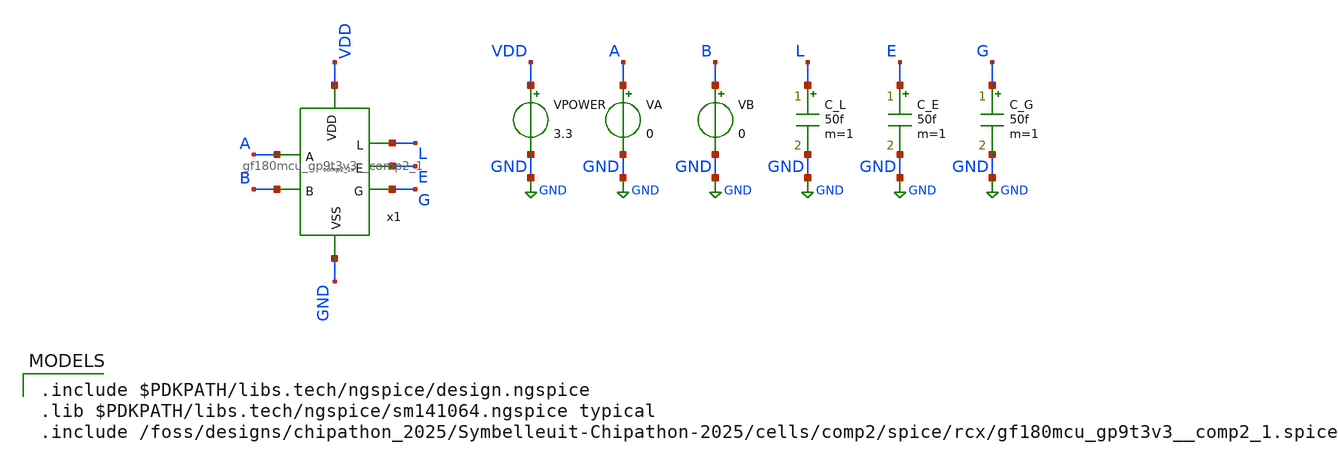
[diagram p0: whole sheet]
** sch_path: cells/comp2/cace/templates/comp2_tb_qpower.sch
**.subckt comp2_tb_qpower
x1 VDD L A E G B GND gf180mcu_gp9t3v3__comp2_1
VPOWER VDD GND 3.3
.save i(vpower)
VA A GND 0
VB B GND 0
C_L L GND 50f m=1
C_E E GND 50f m=1
C_G G GND 50f m=1
**** begin user architecture code

.include $PDKPATH/libs.tech/ngspice/design.ngspice
.lib $PDKPATH/libs.tech/ngspice/sm141064.ngspice typical
.include /foss/designs/chipathon_2025/Symbelleuit-Chipathon-2025/cells/comp2/spice/rcx/gf180mcu_gp9t3v3__comp2_1.spice


* CACE Quiescent Static Power Simulation
.control
  dc VA 0 3.3 3.3 VB 0 3.3 3.3
  let iddq = abs(i(VPOWER))
  let iddq_max = vecmax(iddq)
  let p_quiescent = iddq_max * 3.3
  print p_quiescent
  echo $&p_quiescent > comp2_tb_qpower_0.data
.endc
.GLOBAL GND


**** end user architecture code
**.ends
.GLOBAL GND
.end
